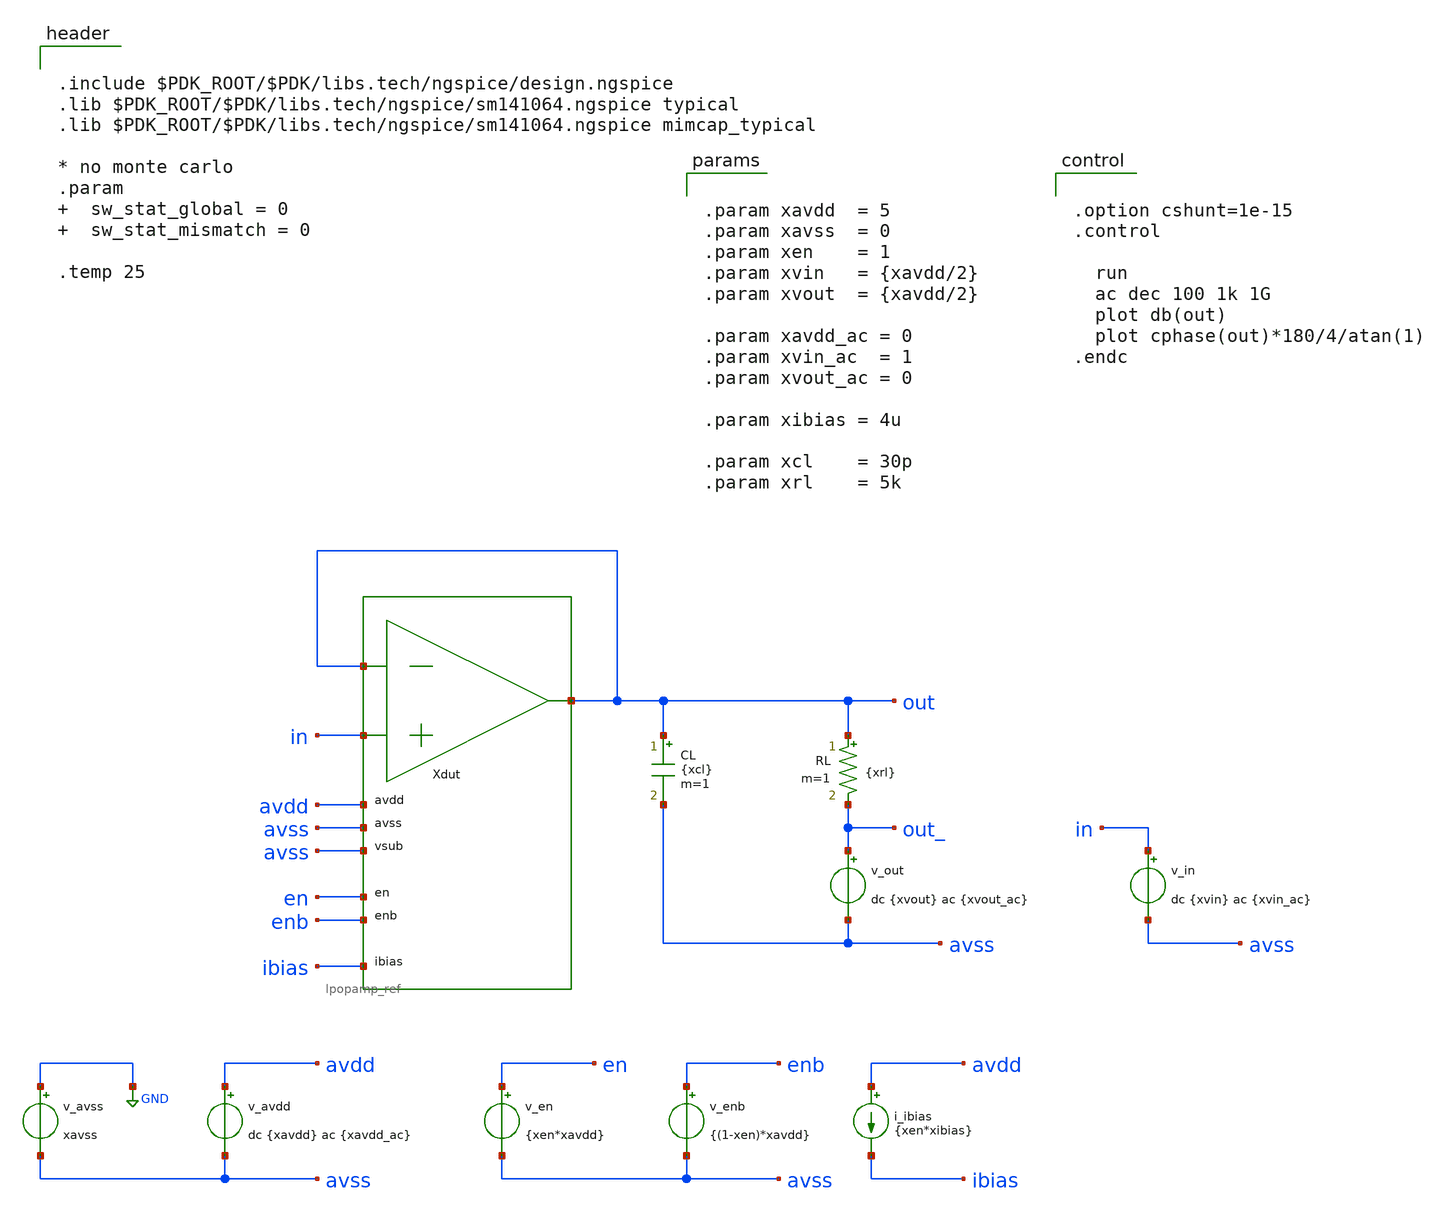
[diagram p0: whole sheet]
** sch_path: xschem/tb_lpopamp_buf_ac.sch
**.subckt tb_lpopamp_buf_ac
Xdut out in out avdd avss avss en enb ibias lpopamp_ref
v_avss GND avss xavss
v_avdd avdd avss dc {xavdd} ac {xavdd_ac}
v_in in avss dc {xvin} ac {xvin_ac}
v_en en avss {xen*xavdd}
v_enb enb avss {(1-xen)*xavdd}
i_ibias avdd ibias {xen*xibias}
CL out avss {xcl} m=1
v_out out_ avss dc {xvout} ac {xvout_ac}
RL out out_ {xrl} m=1
**** begin user architecture code


.include $PDK_ROOT/$PDK/libs.tech/ngspice/design.ngspice
.lib $PDK_ROOT/$PDK/libs.tech/ngspice/sm141064.ngspice typical
.lib $PDK_ROOT/$PDK/libs.tech/ngspice/sm141064.ngspice mimcap_typical

* no monte carlo
.param   sw_stat_global = 0   sw_stat_mismatch = 0

.temp 25




.option cshunt=1e-15
.control

  run
  ac dec 100 1k 1G
  plot db(out)
  plot cphase(out)*180/4/atan(1)
.endc




.param xavdd  = 5
.param xavss  = 0
.param xen    = 1
.param xvin   = {xavdd/2}
.param xvout  = {xavdd/2}

.param xavdd_ac = 0
.param xvin_ac  = 1
.param xvout_ac = 0

.param xibias = 4u

.param xcl    = 30p
.param xrl    = 5k


**** end user architecture code
**.ends
.GLOBAL GND
.end
